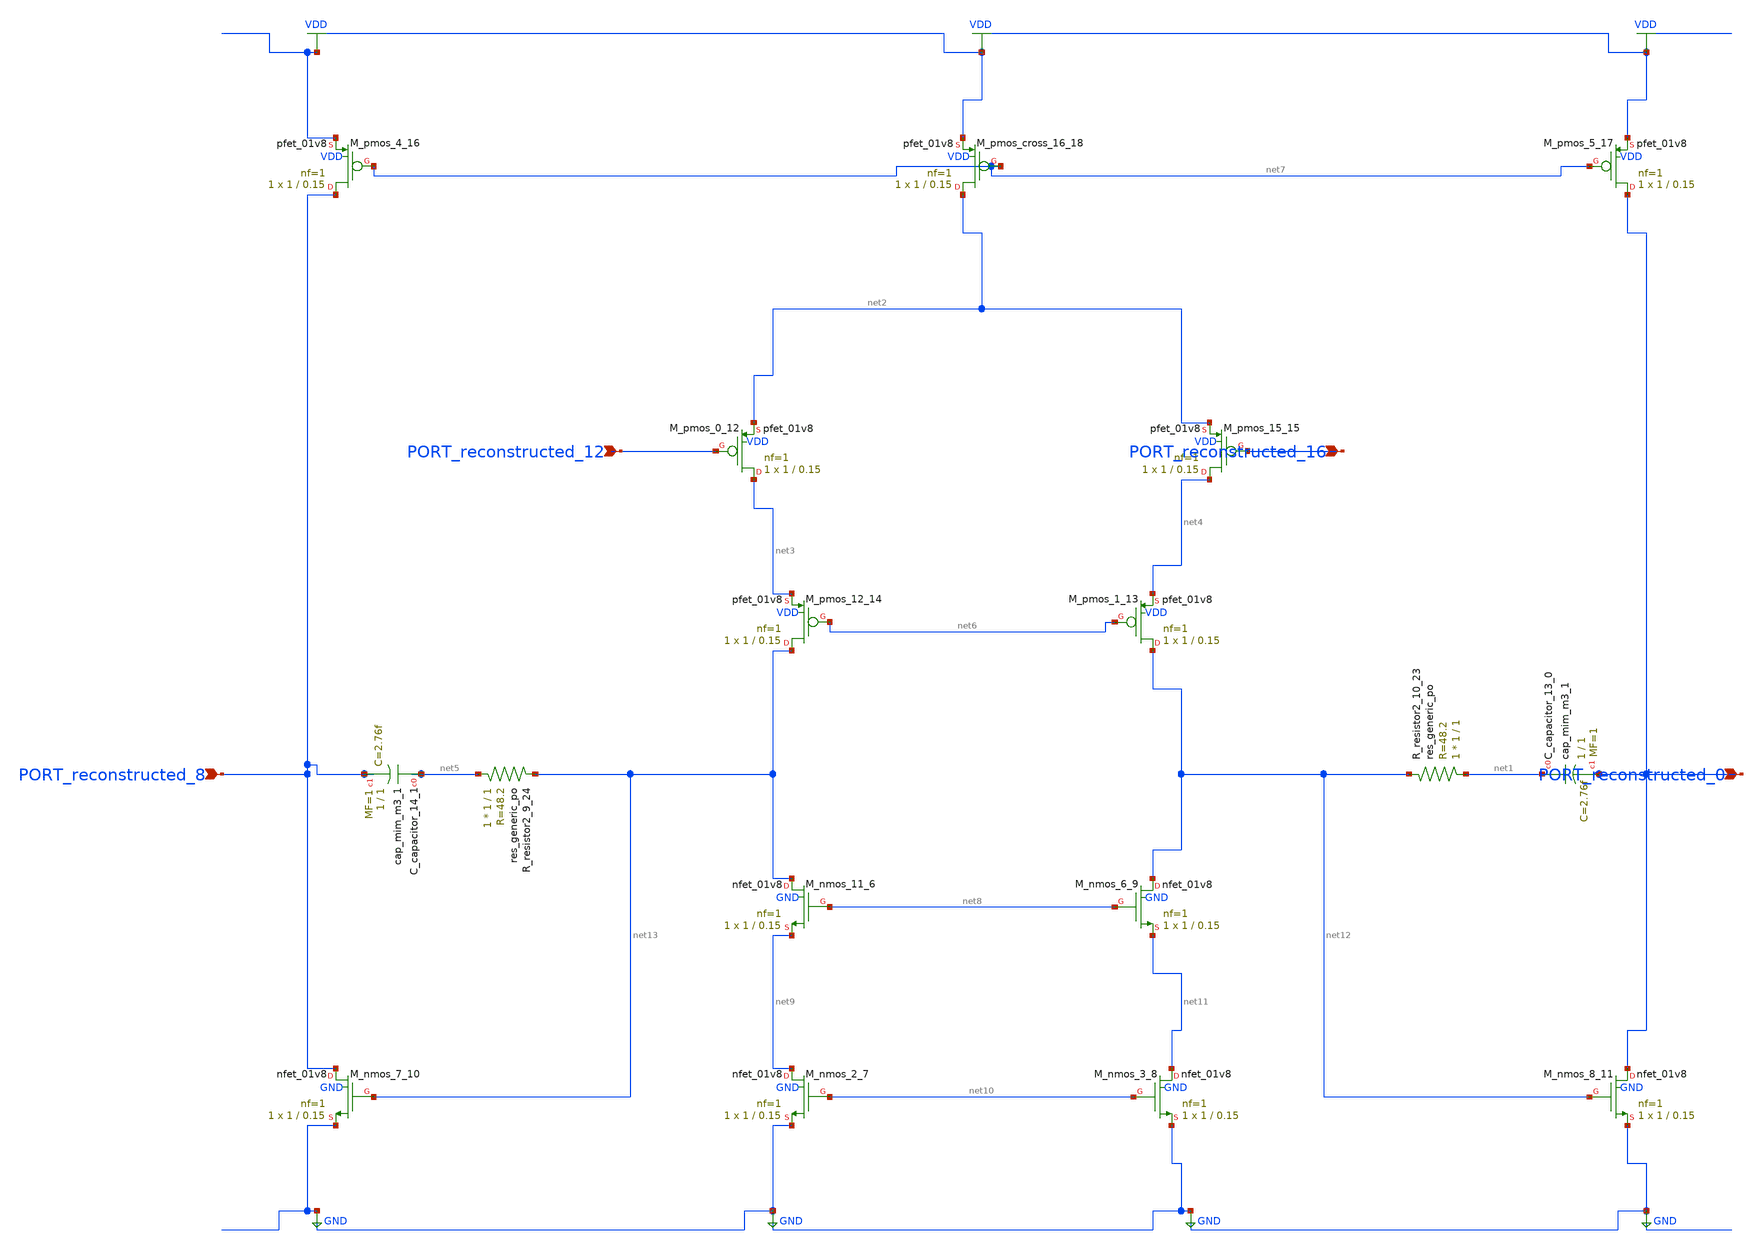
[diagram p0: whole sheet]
** sch_path: schematics/Image2Net/074.sch
**.subckt 074 PORT_reconstructed_12 PORT_reconstructed_16 PORT_reconstructed_0 PORT_reconstructed_8
*.ipin PORT_reconstructed_12
*.ipin PORT_reconstructed_16
*.ipin PORT_reconstructed_0
*.ipin PORT_reconstructed_8
XC_capacitor_13_0 net1 PORT_reconstructed_0 sky130_fd_pr__cap_mim_m3_1 W=1 L=1 MF=1 m=1
XC_capacitor_14_1 net5 PORT_reconstructed_8 sky130_fd_pr__cap_mim_m3_1 W=1 L=1 MF=1 m=1
XM_nmos_11_6 net13 net8 net9 GND sky130_fd_pr__nfet_01v8 L=0.15 W=1 nf=1 ad='int((1 + 1)/2) * 1 / 1 * 0.29'
+ as='int((1 + 2)/2) * 1 / 1 * 0.29' pd='2*int((1 + 1)/2) * (1 / 1 + 0.29)' ps='2*int((1 + 2)/2) * (1 / 1 + 0.29)'
+ nrd='0.29 / 1 ' nrs='0.29 / 1 ' sa=0 sb=0 sd=0 mult=1 m=1
XM_nmos_2_7 net9 net10 GND GND sky130_fd_pr__nfet_01v8 L=0.15 W=1 nf=1 ad='int((1 + 1)/2) * 1 / 1 * 0.29'
+ as='int((1 + 2)/2) * 1 / 1 * 0.29' pd='2*int((1 + 1)/2) * (1 / 1 + 0.29)' ps='2*int((1 + 2)/2) * (1 / 1 + 0.29)'
+ nrd='0.29 / 1 ' nrs='0.29 / 1 ' sa=0 sb=0 sd=0 mult=1 m=1
XM_nmos_3_8 net11 net10 GND GND sky130_fd_pr__nfet_01v8 L=0.15 W=1 nf=1 ad='int((1 + 1)/2) * 1 / 1 * 0.29'
+ as='int((1 + 2)/2) * 1 / 1 * 0.29' pd='2*int((1 + 1)/2) * (1 / 1 + 0.29)' ps='2*int((1 + 2)/2) * (1 / 1 + 0.29)'
+ nrd='0.29 / 1 ' nrs='0.29 / 1 ' sa=0 sb=0 sd=0 mult=1 m=1
XM_nmos_6_9 net12 net8 net11 GND sky130_fd_pr__nfet_01v8 L=0.15 W=1 nf=1 ad='int((1 + 1)/2) * 1 / 1 * 0.29'
+ as='int((1 + 2)/2) * 1 / 1 * 0.29' pd='2*int((1 + 1)/2) * (1 / 1 + 0.29)' ps='2*int((1 + 2)/2) * (1 / 1 + 0.29)'
+ nrd='0.29 / 1 ' nrs='0.29 / 1 ' sa=0 sb=0 sd=0 mult=1 m=1
XM_nmos_7_10 PORT_reconstructed_8 net13 GND GND sky130_fd_pr__nfet_01v8 L=0.15 W=1 nf=1 ad='int((1 + 1)/2) * 1 / 1 * 0.29'
+ as='int((1 + 2)/2) * 1 / 1 * 0.29' pd='2*int((1 + 1)/2) * (1 / 1 + 0.29)' ps='2*int((1 + 2)/2) * (1 / 1 + 0.29)'
+ nrd='0.29 / 1 ' nrs='0.29 / 1 ' sa=0 sb=0 sd=0 mult=1 m=1
XM_nmos_8_11 PORT_reconstructed_0 net12 GND GND sky130_fd_pr__nfet_01v8 L=0.15 W=1 nf=1 ad='int((1 + 1)/2) * 1 / 1 * 0.29'
+ as='int((1 + 2)/2) * 1 / 1 * 0.29' pd='2*int((1 + 1)/2) * (1 / 1 + 0.29)' ps='2*int((1 + 2)/2) * (1 / 1 + 0.29)'
+ nrd='0.29 / 1 ' nrs='0.29 / 1 ' sa=0 sb=0 sd=0 mult=1 m=1
XM_pmos_0_12 net3 PORT_reconstructed_12 net2 VDD sky130_fd_pr__pfet_01v8 L=0.15 W=1 nf=1 ad='int((1 + 1)/2) * 1 / 1 * 0.29'
+ as='int((1 + 2)/2) * 1 / 1 * 0.29' pd='2*int((1 + 1)/2) * (1 / 1 + 0.29)' ps='2*int((1 + 2)/2) * (1 / 1 + 0.29)'
+ nrd='0.29 / 1 ' nrs='0.29 / 1 ' sa=0 sb=0 sd=0 mult=1 m=1
XM_pmos_1_13 net12 net6 net4 VDD sky130_fd_pr__pfet_01v8 L=0.15 W=1 nf=1 ad='int((1 + 1)/2) * 1 / 1 * 0.29'
+ as='int((1 + 2)/2) * 1 / 1 * 0.29' pd='2*int((1 + 1)/2) * (1 / 1 + 0.29)' ps='2*int((1 + 2)/2) * (1 / 1 + 0.29)'
+ nrd='0.29 / 1 ' nrs='0.29 / 1 ' sa=0 sb=0 sd=0 mult=1 m=1
XM_pmos_12_14 net13 net6 net3 VDD sky130_fd_pr__pfet_01v8 L=0.15 W=1 nf=1 ad='int((1 + 1)/2) * 1 / 1 * 0.29'
+ as='int((1 + 2)/2) * 1 / 1 * 0.29' pd='2*int((1 + 1)/2) * (1 / 1 + 0.29)' ps='2*int((1 + 2)/2) * (1 / 1 + 0.29)'
+ nrd='0.29 / 1 ' nrs='0.29 / 1 ' sa=0 sb=0 sd=0 mult=1 m=1
XM_pmos_15_15 net4 PORT_reconstructed_16 net2 VDD sky130_fd_pr__pfet_01v8 L=0.15 W=1 nf=1 ad='int((1 + 1)/2) * 1 / 1 * 0.29'
+ as='int((1 + 2)/2) * 1 / 1 * 0.29' pd='2*int((1 + 1)/2) * (1 / 1 + 0.29)' ps='2*int((1 + 2)/2) * (1 / 1 + 0.29)'
+ nrd='0.29 / 1 ' nrs='0.29 / 1 ' sa=0 sb=0 sd=0 mult=1 m=1
XM_pmos_4_16 PORT_reconstructed_8 net7 VDD VDD sky130_fd_pr__pfet_01v8 L=0.15 W=1 nf=1 ad='int((1 + 1)/2) * 1 / 1 * 0.29'
+ as='int((1 + 2)/2) * 1 / 1 * 0.29' pd='2*int((1 + 1)/2) * (1 / 1 + 0.29)' ps='2*int((1 + 2)/2) * (1 / 1 + 0.29)'
+ nrd='0.29 / 1 ' nrs='0.29 / 1 ' sa=0 sb=0 sd=0 mult=1 m=1
XM_pmos_5_17 PORT_reconstructed_0 net7 VDD VDD sky130_fd_pr__pfet_01v8 L=0.15 W=1 nf=1 ad='int((1 + 1)/2) * 1 / 1 * 0.29'
+ as='int((1 + 2)/2) * 1 / 1 * 0.29' pd='2*int((1 + 1)/2) * (1 / 1 + 0.29)' ps='2*int((1 + 2)/2) * (1 / 1 + 0.29)'
+ nrd='0.29 / 1 ' nrs='0.29 / 1 ' sa=0 sb=0 sd=0 mult=1 m=1
XM_pmos_cross_16_18 net2 net7 VDD VDD sky130_fd_pr__pfet_01v8 L=0.15 W=1 nf=1 ad='int((1 + 1)/2) * 1 / 1 * 0.29'
+ as='int((1 + 2)/2) * 1 / 1 * 0.29' pd='2*int((1 + 1)/2) * (1 / 1 + 0.29)' ps='2*int((1 + 2)/2) * (1 / 1 + 0.29)'
+ nrd='0.29 / 1 ' nrs='0.29 / 1 ' sa=0 sb=0 sd=0 mult=1 m=1
XR_resistor2_10_23 net1 net12 sky130_fd_pr__res_generic_po W=1 L=1 m=1
XR_resistor2_9_24 net5 net13 sky130_fd_pr__res_generic_po W=1 L=1 m=1
**.ends
.GLOBAL GND
.GLOBAL VDD
.end
